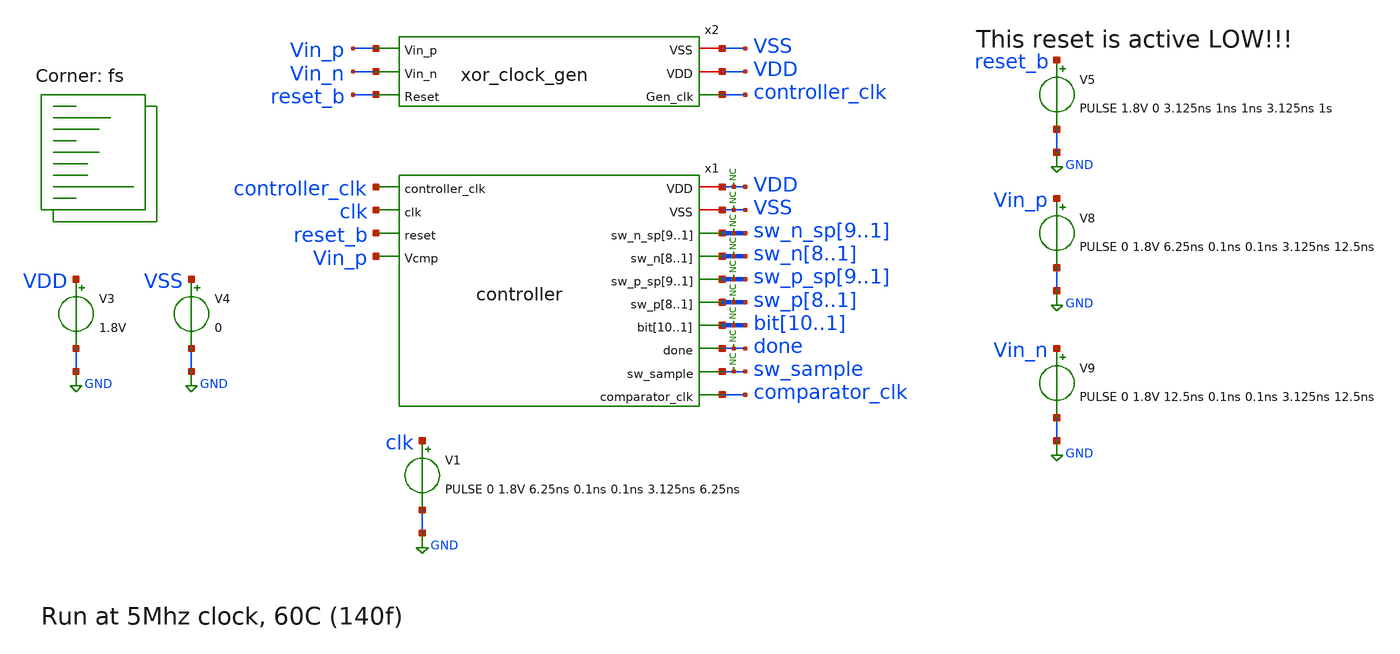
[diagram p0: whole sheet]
** sch_path: xschem/tests/controller/controller_corner_fs_test.sch
**.subckt controller_corner_fs_test
V3 VDD GND 1.8V
V4 VSS GND 0
V1 clk GND PULSE 0 1.8V 6.25ns 0.1ns 0.1ns 3.125ns 6.25ns
V5 reset_b GND PULSE 1.8V 0 3.125ns 1ns 1ns 3.125ns 1s
V8 Vin_p GND PULSE 0 1.8V 6.25ns 0.1ns 0.1ns 3.125ns 12.5ns
x1 VDD controller_clk VSS sw_n_sp9 sw_n_sp8 sw_n_sp7 sw_n_sp6 sw_n_sp5 sw_n_sp4 sw_n_sp3 sw_n_sp2
+ sw_n_sp1 clk sw_n8 sw_n7 sw_n6 sw_n5 sw_n4 sw_n3 sw_n2 sw_n1 reset_b Vin_p sw_p_sp9 sw_p_sp8 sw_p_sp7
+ sw_p_sp6 sw_p_sp5 sw_p_sp4 sw_p_sp3 sw_p_sp2 sw_p_sp1 sw_p8 sw_p7 sw_p6 sw_p5 sw_p4 sw_p3 sw_p2 sw_p1 bit10
+ bit9 bit8 bit7 bit6 bit5 bit4 bit3 bit2 bit1 done sw_sample comparator_clk controller
x2 VSS Vin_p VDD Vin_n controller_clk reset_b xor_clock_gen
* noconn VDD
* noconn VSS
* noconn sw_n_sp[9..1]
* noconn sw_n[8..1]
* noconn sw_p_sp[9..1]
* noconn sw_p[8..1]
* noconn bit[10..1]
* noconn done
* noconn sw_sample
V9 Vin_n GND PULSE 0 1.8V 12.5ns 0.1ns 0.1ns 3.125ns 12.5ns
**** begin user architecture code
 *.lib $::SKYWATER_MODELS/sky130.lib.spice tt
.include $::SKYWATER_STDCELLS/sky130_fd_sc_hd.spice


.options acct list
.temp 60
*vvcc VDD 0 dc 1.8
*vvss VSS 0 0
.control
tran 0.1n 220n
*plot RST_PLS clk+2 Pulse+4
plot done-4  sw_n_sp1 sw_n_sp2+2 sw_n_sp3+4 sw_n_sp4+6 sw_n_sp5+8 sw_n_sp6+10 sw_n_sp7+12
+ sw_n_sp8+14 sw_n_sp9+16 Vin_p+18 clk+20
plot done-4  sw_p_sp1 sw_p_sp2+2 sw_p_sp3+4 sw_p_sp4+6 sw_p_sp5+8 sw_p_sp6+10 sw_p_sp7+12
+ sw_p_sp8+14 sw_p_sp9+16 Vin_p+18 clk+20
plot done-4  sw_n1 sw_n2+2 sw_n3+4 sw_n4+6 sw_n5+8 sw_n6+10 sw_n7+12 sw_n8+14 Vin_p+16 clk+18
plot done-4  sw_p1 sw_p2+2 sw_p3+4 sw_p4+6 sw_p5+8 sw_p6+10 sw_p7+12 sw_p8+14 Vin_p+16 clk+18
plot done-4 bit1 bit2+2 bit3+4 bit4+6 bit5+8 bit6+10 bit7+12 bit8+14 bit9+16 bit10+18

plot done-4  sw_n_sp1 sw_n_sp2+2 sw_n_sp3+4 sw_n_sp4+6 sw_n_sp5+8 sw_n_sp6+10 sw_n_sp7+12
+ sw_n_sp8+14 sw_n_sp9+16 Vin_q+18 clk+20 sw_n1 sw_n2+2 sw_n3+4 sw_n4+6 sw_n5+8 sw_n6+10 sw_n7+12 sw_n8+14

plot done-4  sw_p_sp1 sw_p_sp2+2 sw_p_sp3+4 sw_p_sp4+6 sw_p_sp5+8 sw_p_sp6+10 sw_p_sp7+12
+ sw_p_sp8+14 sw_p_sp9+16 Vin_q+18 clk+20 sw_p1 sw_p2+2 sw_p3+4 sw_p4+6 sw_p5+8 sw_p6+10 sw_p7+12 sw_p8+14

plot clk reset_b+2 x1.cycle0+4 x1.cycle1+6 x1.cycle2+8 x1.cycle16+10 x1.cycle17+12 x1.cycle18+14
+ sw_sample+16 vin_p+18

plot reset_b-2 clk vin_p gen_clk

.endc


.lib $::SKYWATER_MODELS/sky130.lib.spice fs
**** end user architecture code
**.ends
.GLOBAL GND
.end
